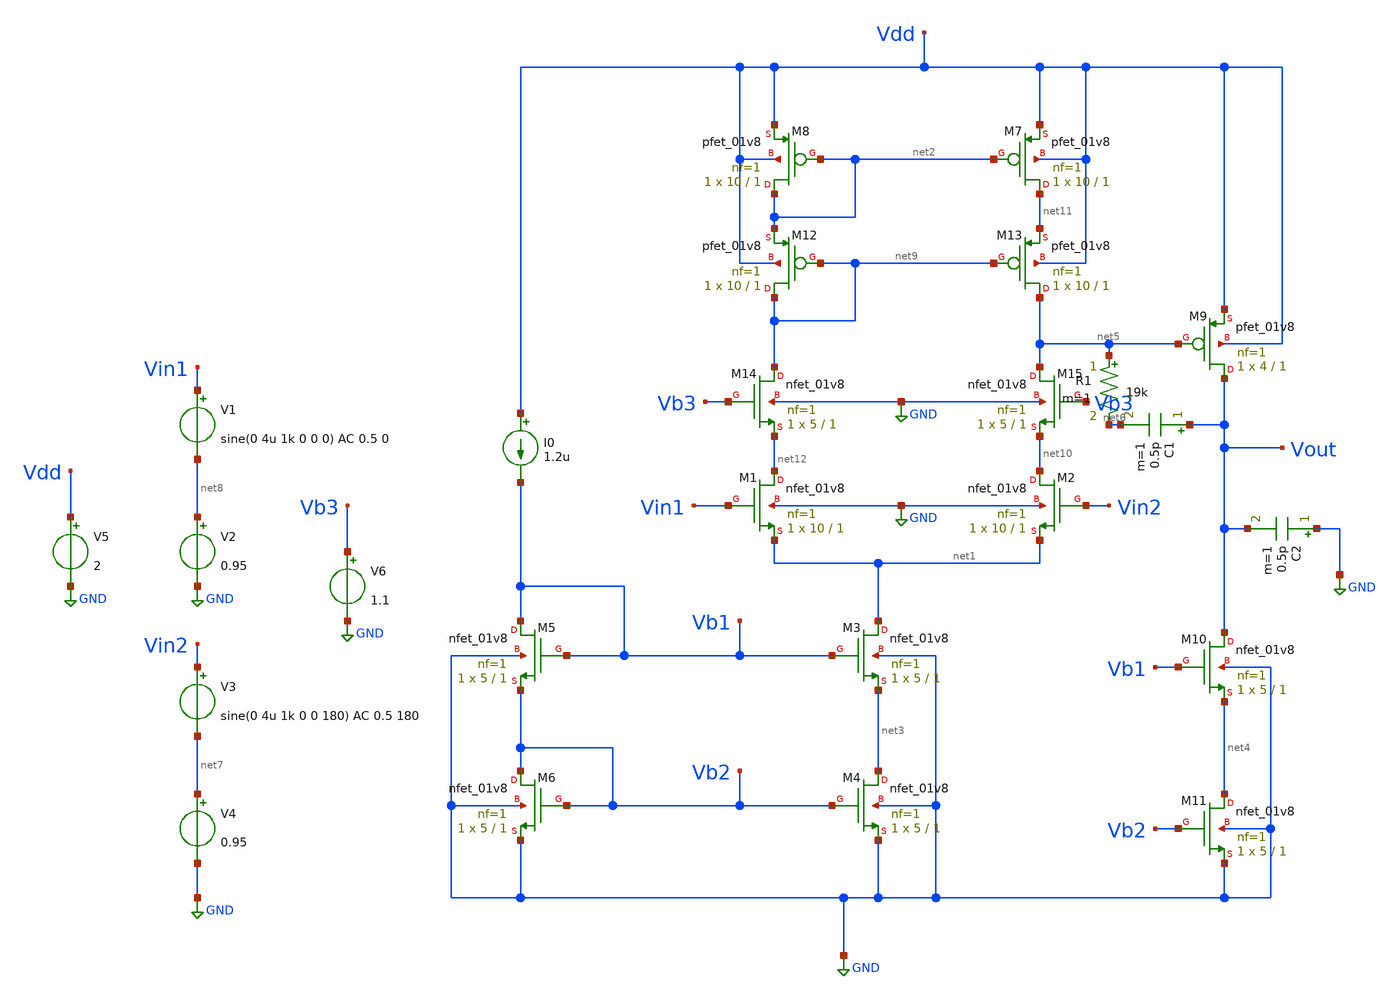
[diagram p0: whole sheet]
** sch_path: dac.sch
**.subckt dac
XM1 net12 Vin1 net1 GND sky130_fd_pr__nfet_01v8 L=1 W=10 nf=1 ad='int((nf+1)/2) * W/nf * 0.29' as='int((nf+2)/2) * W/nf * 0.29'
+ pd='2*int((nf+1)/2) * (W/nf + 0.29)' ps='2*int((nf+2)/2) * (W/nf + 0.29)' nrd='0.29 / W' nrs='0.29 / W'
+ sa=0 sb=0 sd=0 mult=1 m=1
XM2 net10 Vin2 net1 GND sky130_fd_pr__nfet_01v8 L=1 W=10 nf=1 ad='int((nf+1)/2) * W/nf * 0.29' as='int((nf+2)/2) * W/nf * 0.29'
+ pd='2*int((nf+1)/2) * (W/nf + 0.29)' ps='2*int((nf+2)/2) * (W/nf + 0.29)' nrd='0.29 / W' nrs='0.29 / W'
+ sa=0 sb=0 sd=0 mult=1 m=1
XM3 net1 Vb1 net3 GND sky130_fd_pr__nfet_01v8 L=1 W=5 nf=1 ad='int((nf+1)/2) * W/nf * 0.29' as='int((nf+2)/2) * W/nf * 0.29'
+ pd='2*int((nf+1)/2) * (W/nf + 0.29)' ps='2*int((nf+2)/2) * (W/nf + 0.29)' nrd='0.29 / W' nrs='0.29 / W'
+ sa=0 sb=0 sd=0 mult=1 m=1
XM4 net3 Vb2 GND GND sky130_fd_pr__nfet_01v8 L=1 W=5 nf=1 ad='int((nf+1)/2) * W/nf * 0.29' as='int((nf+2)/2) * W/nf * 0.29'
+ pd='2*int((nf+1)/2) * (W/nf + 0.29)' ps='2*int((nf+2)/2) * (W/nf + 0.29)' nrd='0.29 / W' nrs='0.29 / W'
+ sa=0 sb=0 sd=0 mult=1 m=1
XM5 Vb1 Vb1 Vb2 GND sky130_fd_pr__nfet_01v8 L=1 W=5 nf=1 ad='int((nf+1)/2) * W/nf * 0.29' as='int((nf+2)/2) * W/nf * 0.29'
+ pd='2*int((nf+1)/2) * (W/nf + 0.29)' ps='2*int((nf+2)/2) * (W/nf + 0.29)' nrd='0.29 / W' nrs='0.29 / W'
+ sa=0 sb=0 sd=0 mult=1 m=1
XM6 Vb2 Vb2 GND GND sky130_fd_pr__nfet_01v8 L=1 W=5 nf=1 ad='int((nf+1)/2) * W/nf * 0.29' as='int((nf+2)/2) * W/nf * 0.29'
+ pd='2*int((nf+1)/2) * (W/nf + 0.29)' ps='2*int((nf+2)/2) * (W/nf + 0.29)' nrd='0.29 / W' nrs='0.29 / W'
+ sa=0 sb=0 sd=0 mult=1 m=1
XM7 net11 net2 Vdd Vdd sky130_fd_pr__pfet_01v8 L=1 W=10 nf=1 ad='int((nf+1)/2) * W/nf * 0.29' as='int((nf+2)/2) * W/nf * 0.29'
+ pd='2*int((nf+1)/2) * (W/nf + 0.29)' ps='2*int((nf+2)/2) * (W/nf + 0.29)' nrd='0.29 / W' nrs='0.29 / W'
+ sa=0 sb=0 sd=0 mult=1 m=1
XM8 net2 net2 Vdd Vdd sky130_fd_pr__pfet_01v8 L=1 W=10 nf=1 ad='int((nf+1)/2) * W/nf * 0.29' as='int((nf+2)/2) * W/nf * 0.29'
+ pd='2*int((nf+1)/2) * (W/nf + 0.29)' ps='2*int((nf+2)/2) * (W/nf + 0.29)' nrd='0.29 / W' nrs='0.29 / W'
+ sa=0 sb=0 sd=0 mult=1 m=1
I0 Vdd Vb1 1.2u
XM9 Vout net5 Vdd Vdd sky130_fd_pr__pfet_01v8 L=1 W=4 nf=1 ad='int((nf+1)/2) * W/nf * 0.29' as='int((nf+2)/2) * W/nf * 0.29'
+ pd='2*int((nf+1)/2) * (W/nf + 0.29)' ps='2*int((nf+2)/2) * (W/nf + 0.29)' nrd='0.29 / W' nrs='0.29 / W'
+ sa=0 sb=0 sd=0 mult=1 m=1
XM10 Vout Vb1 net4 GND sky130_fd_pr__nfet_01v8 L=1 W=5 nf=1 ad='int((nf+1)/2) * W/nf * 0.29' as='int((nf+2)/2) * W/nf * 0.29'
+ pd='2*int((nf+1)/2) * (W/nf + 0.29)' ps='2*int((nf+2)/2) * (W/nf + 0.29)' nrd='0.29 / W' nrs='0.29 / W'
+ sa=0 sb=0 sd=0 mult=1 m=1
XM11 net4 Vb2 GND GND sky130_fd_pr__nfet_01v8 L=1 W=5 nf=1 ad='int((nf+1)/2) * W/nf * 0.29' as='int((nf+2)/2) * W/nf * 0.29'
+ pd='2*int((nf+1)/2) * (W/nf + 0.29)' ps='2*int((nf+2)/2) * (W/nf + 0.29)' nrd='0.29 / W' nrs='0.29 / W'
+ sa=0 sb=0 sd=0 mult=1 m=1
C1 Vout net6 0.5p m=1
C2 GND Vout 0.5p m=1
V1 Vin1 net8 sine(0 4u 1k 0 0 0) AC 0.5 0
V2 net8 GND 0.95
V3 Vin2 net7 sine(0 4u 1k 0 0 180) AC 0.5 180
V4 net7 GND 0.95
V5 Vdd GND 2
XM12 net9 net9 net2 Vdd sky130_fd_pr__pfet_01v8 L=1 W=10 nf=1 ad='int((nf+1)/2) * W/nf * 0.29' as='int((nf+2)/2) * W/nf * 0.29'
+ pd='2*int((nf+1)/2) * (W/nf + 0.29)' ps='2*int((nf+2)/2) * (W/nf + 0.29)' nrd='0.29 / W' nrs='0.29 / W'
+ sa=0 sb=0 sd=0 mult=1 m=1
XM13 net5 net9 net11 Vdd sky130_fd_pr__pfet_01v8 L=1 W=10 nf=1 ad='int((nf+1)/2) * W/nf * 0.29' as='int((nf+2)/2) * W/nf * 0.29'
+ pd='2*int((nf+1)/2) * (W/nf + 0.29)' ps='2*int((nf+2)/2) * (W/nf + 0.29)' nrd='0.29 / W' nrs='0.29 / W'
+ sa=0 sb=0 sd=0 mult=1 m=1
XM14 net9 Vb3 net12 GND sky130_fd_pr__nfet_01v8 L=1 W=5 nf=1 ad='int((nf+1)/2) * W/nf * 0.29' as='int((nf+2)/2) * W/nf * 0.29'
+ pd='2*int((nf+1)/2) * (W/nf + 0.29)' ps='2*int((nf+2)/2) * (W/nf + 0.29)' nrd='0.29 / W' nrs='0.29 / W'
+ sa=0 sb=0 sd=0 mult=1 m=1
XM15 net5 Vb3 net10 GND sky130_fd_pr__nfet_01v8 L=1 W=5 nf=1 ad='int((nf+1)/2) * W/nf * 0.29' as='int((nf+2)/2) * W/nf * 0.29'
+ pd='2*int((nf+1)/2) * (W/nf + 0.29)' ps='2*int((nf+2)/2) * (W/nf + 0.29)' nrd='0.29 / W' nrs='0.29 / W'
+ sa=0 sb=0 sd=0 mult=1 m=1
V6 Vb3 GND 1.1
R1 net5 net6 19k m=1
**** begin user architecture code


.ac dec 10 1 10G
.tran 10u 5m

# Parameter-aware Subcircuit wrapper for NFET
.subckt sky130_fd_pr__nfet_01v8 d g s b w=1 l=0.15 nf=1 mult=1 ad=0 as=0 pd=0 ps=0 nrd=0 nrs=0 sa=0
+ sb=0 sd=0
.model ideal_n nmos vto=0.7 kp=160e-6
m1 d g s b ideal_n w={w} l={l}
.ends

# Parameter-aware Subcircuit wrapper for PFET
.subckt sky130_fd_pr__pfet_01v8 d g s b w=1 l=0.15 nf=1 mult=1 ad=0 as=0 pd=0 ps=0 nrd=0 nrs=0 sa=0
+ sb=0 sd=0
.model ideal_p pmos vto=-0.7 kp=45e-6
m1 d g s b ideal_p w={w} l={l}
.ends

.control
  run
  set color0=white
  set color1=black

  ; --- 1. Plot Transient Waveform ---
  setplot tran1
  plot v(Vin1) v(Vout)

  ; --- 2. Plot AC Bode Response (Gain & Phase) ---
  setplot ac1
  let phase_deg = (180/PI) * cph(v(Vout))
  let gain_db = db(v(Vout))
  plot gain_db phase_deg ylimit -60 100

  ; --- 3. Measure Bandwidth & Phase Margin in Console ---
  meas ac gbw when gain_db=0
  meas ac phase_at_gbw find phase_deg when gain_db=0
  let phase_margin = 180 + phase_at_gbw
  print gbw phase_margin
.endc


**** end user architecture code
**.ends
.GLOBAL GND
.end
